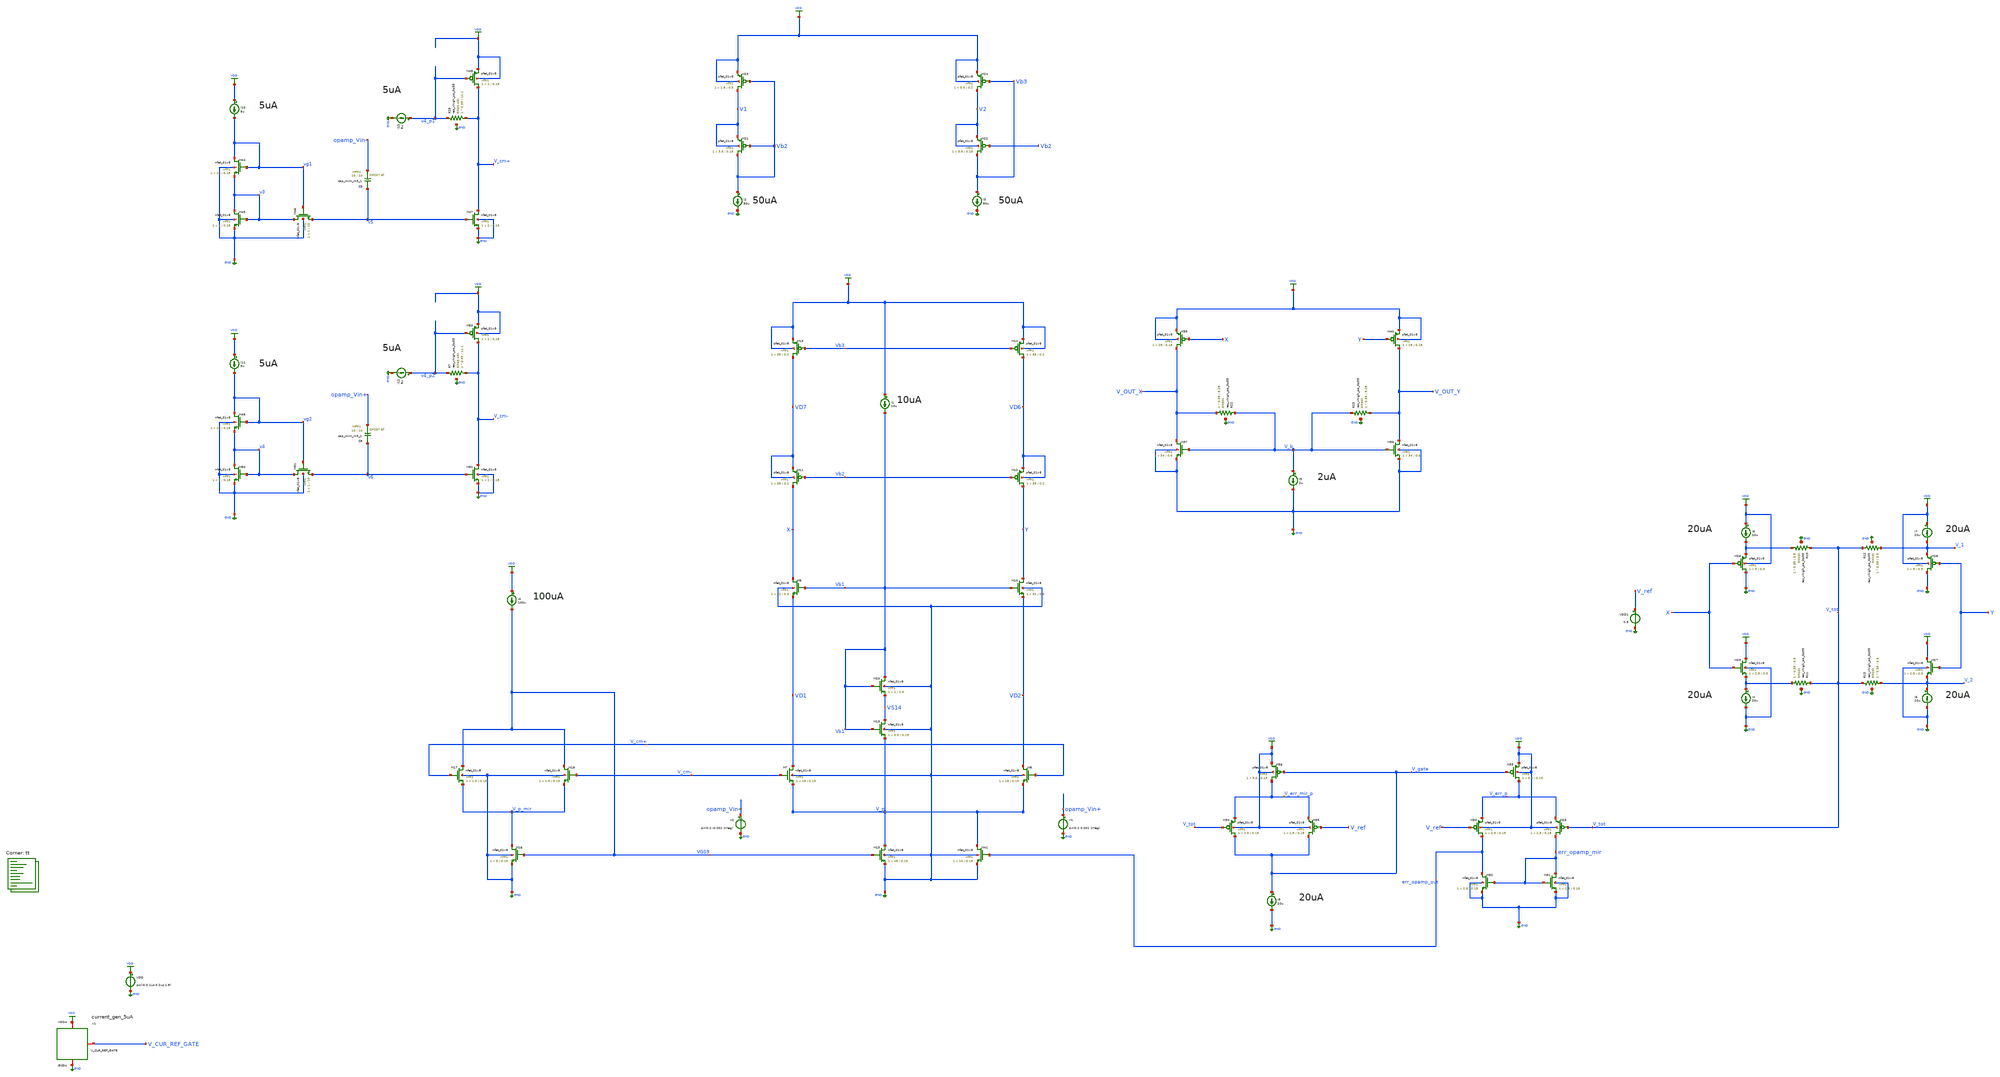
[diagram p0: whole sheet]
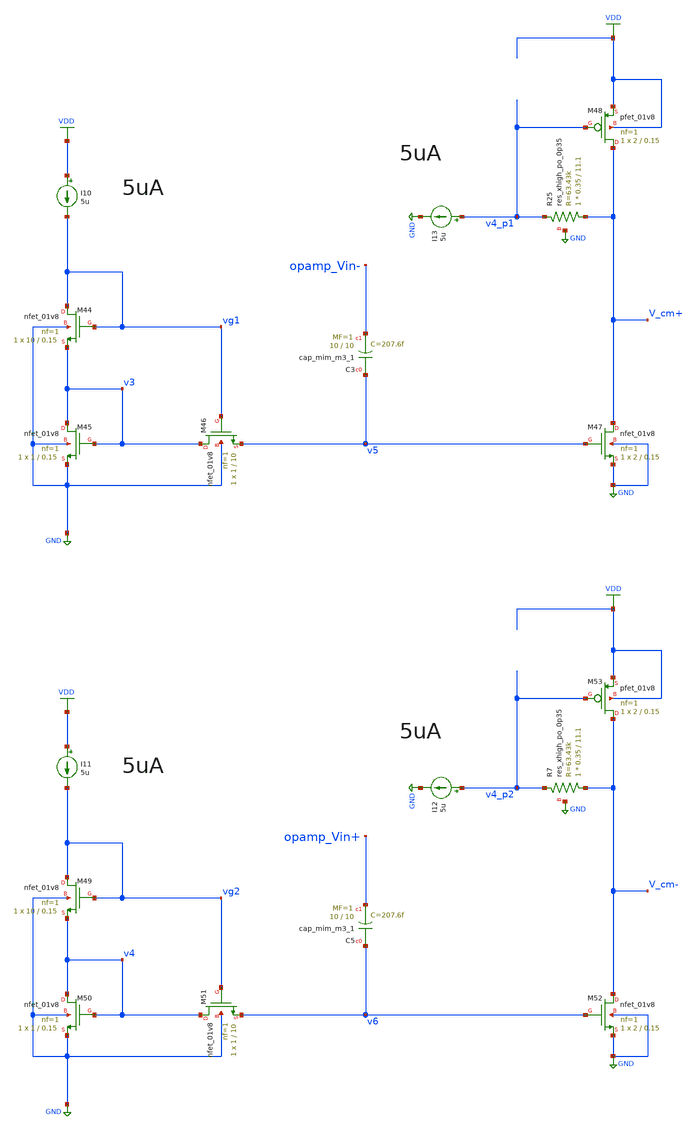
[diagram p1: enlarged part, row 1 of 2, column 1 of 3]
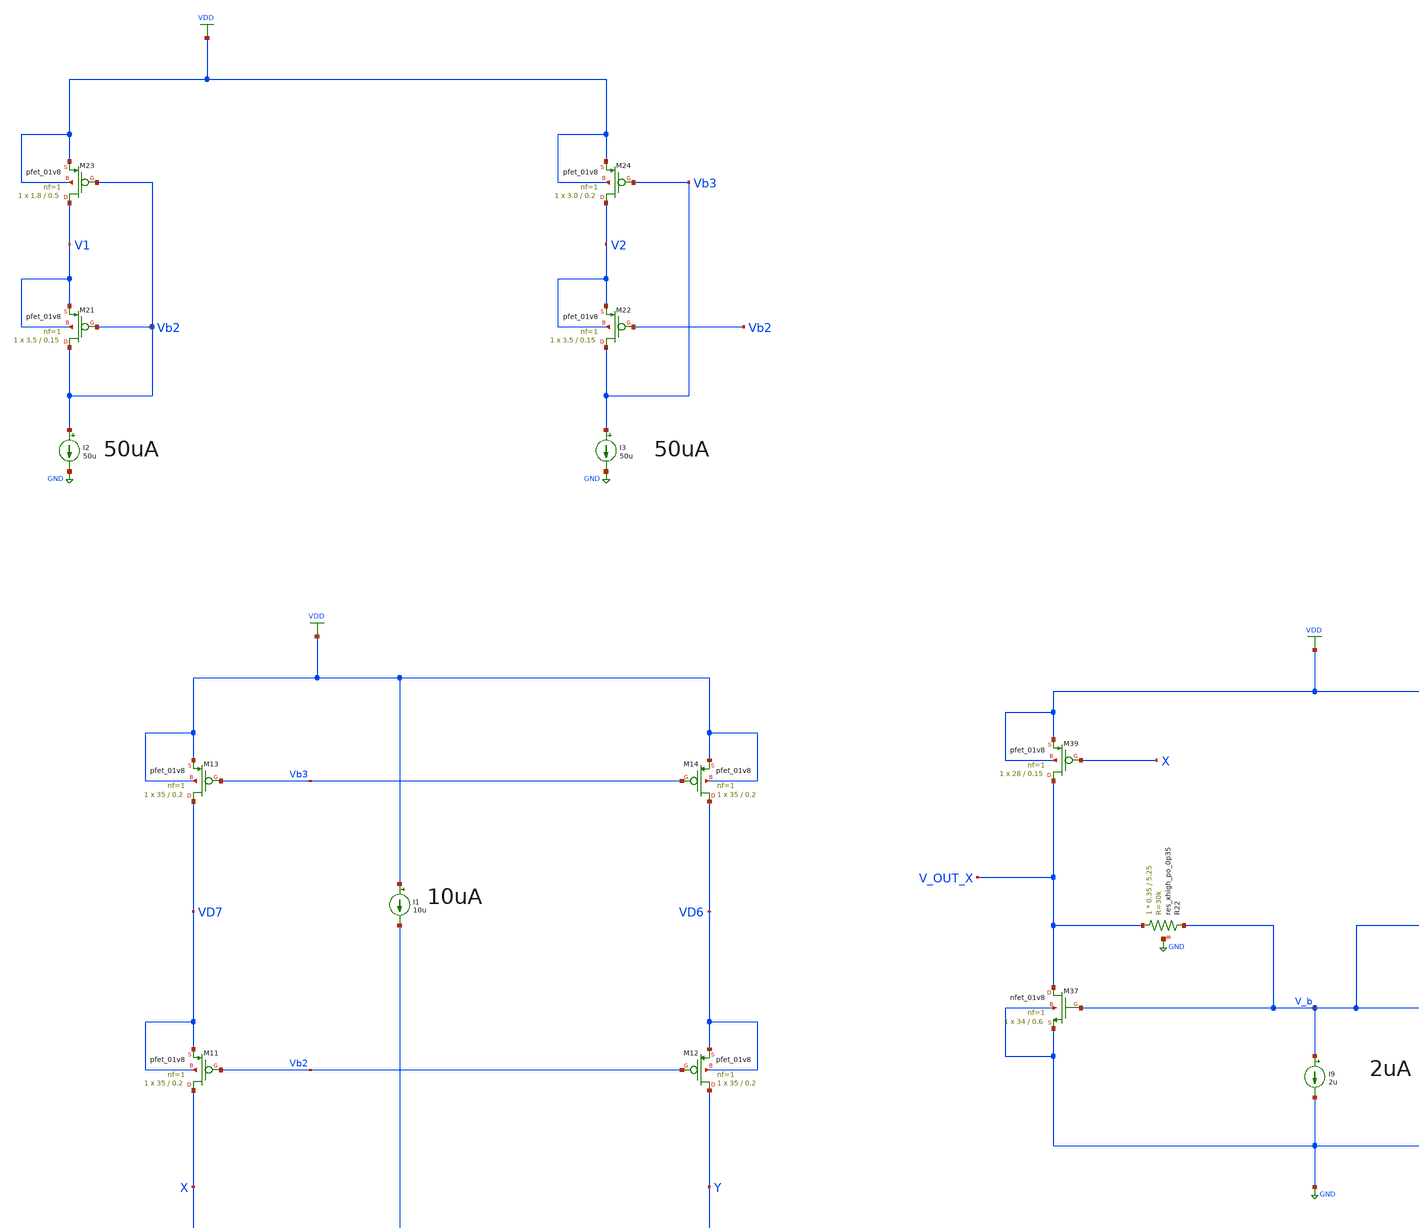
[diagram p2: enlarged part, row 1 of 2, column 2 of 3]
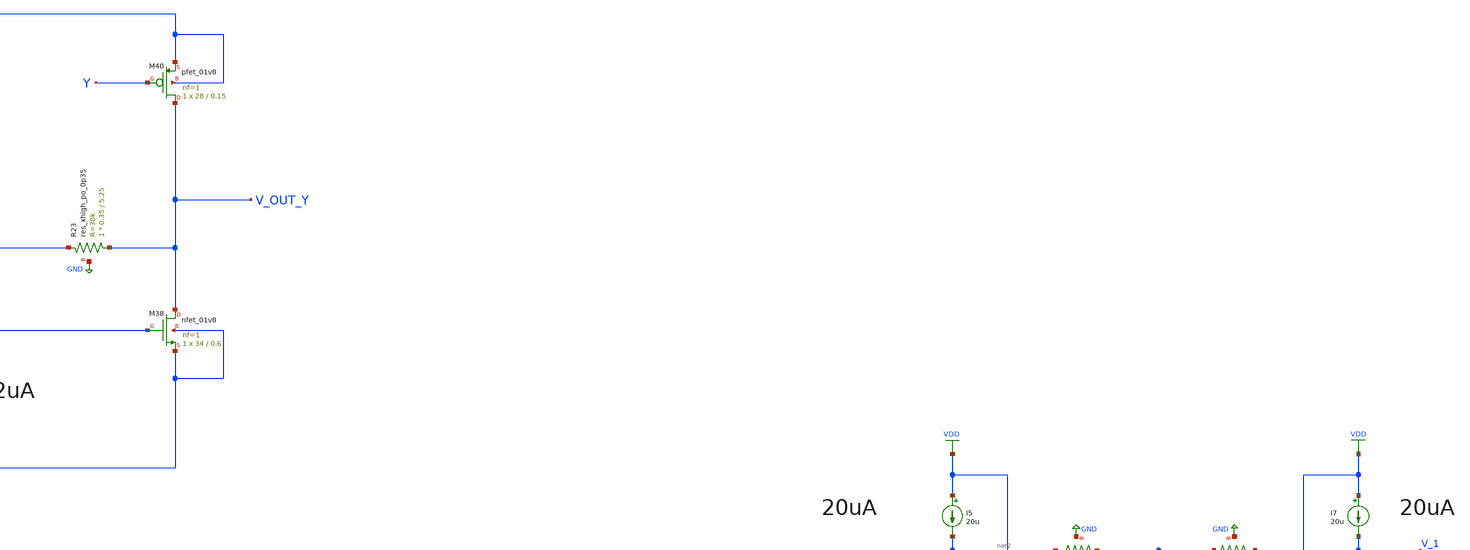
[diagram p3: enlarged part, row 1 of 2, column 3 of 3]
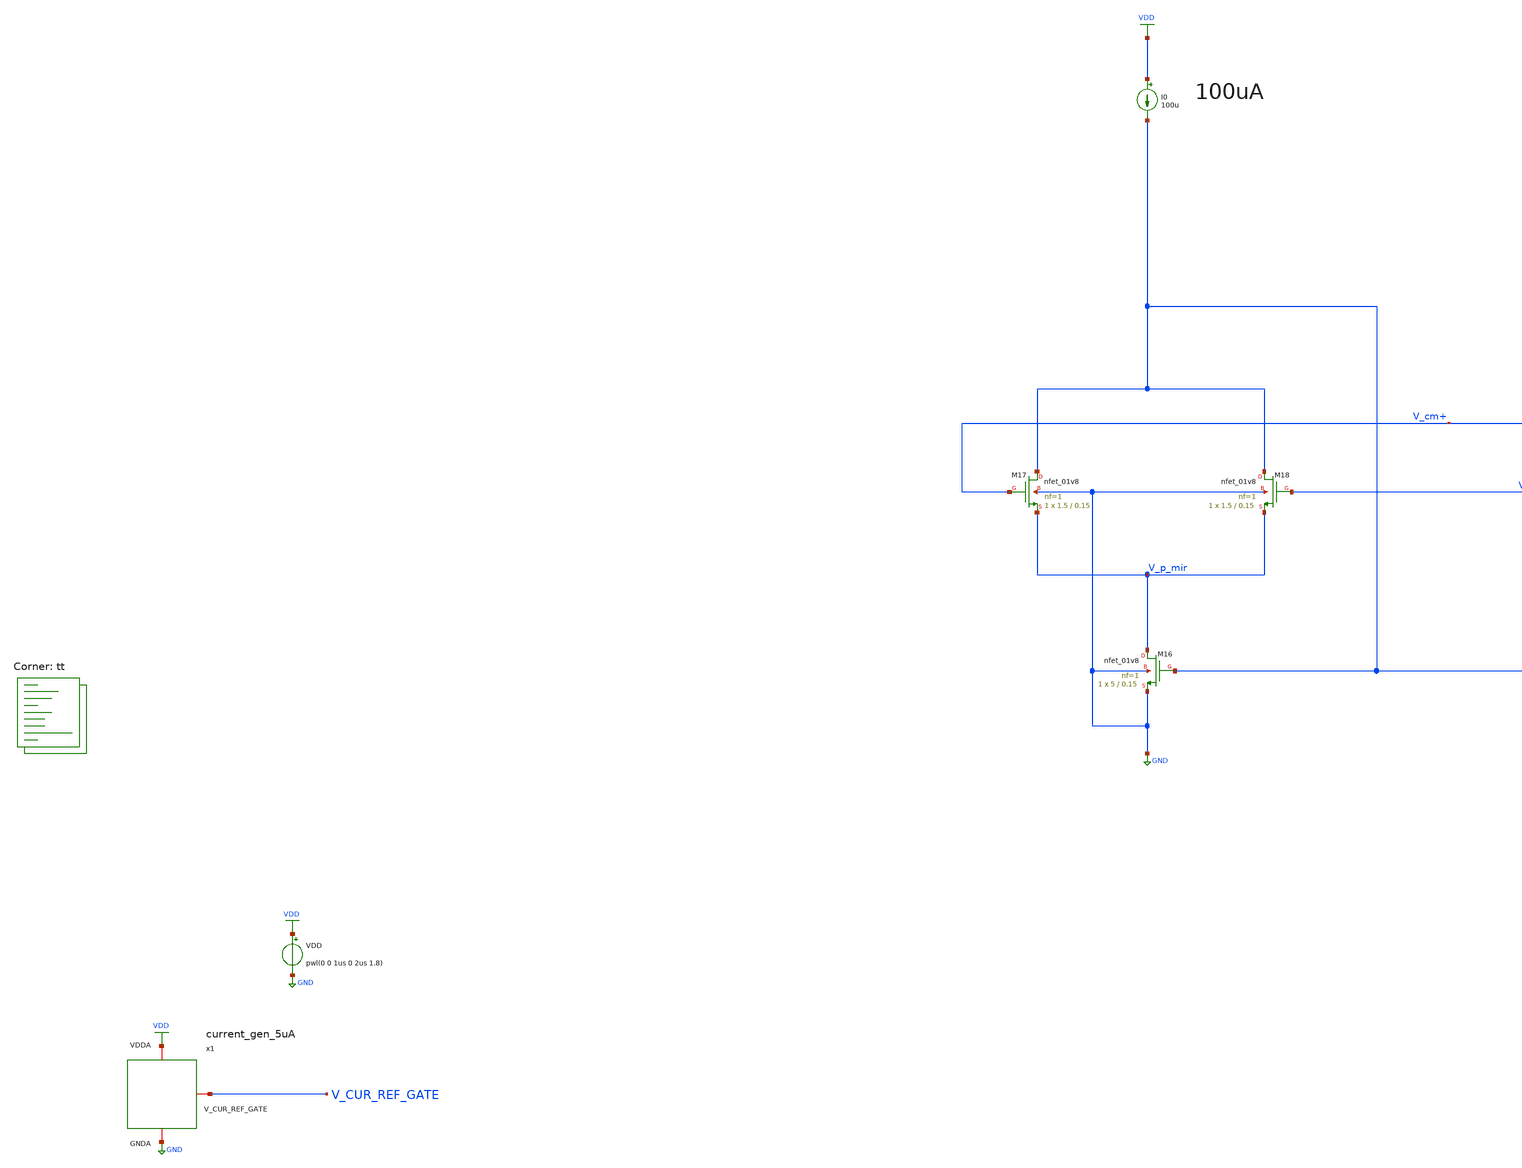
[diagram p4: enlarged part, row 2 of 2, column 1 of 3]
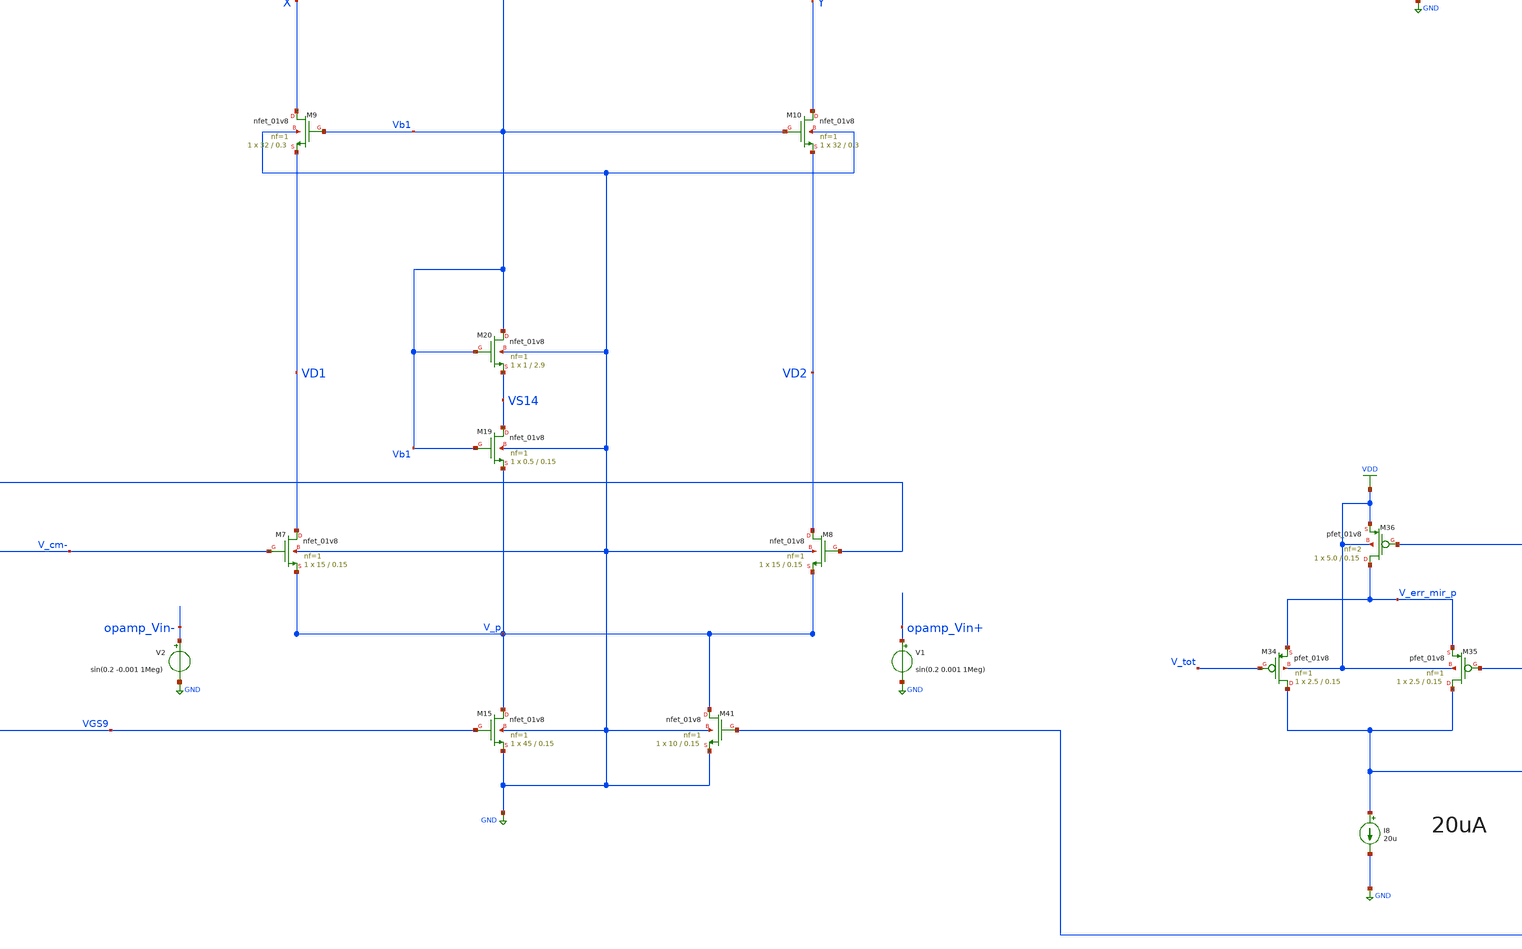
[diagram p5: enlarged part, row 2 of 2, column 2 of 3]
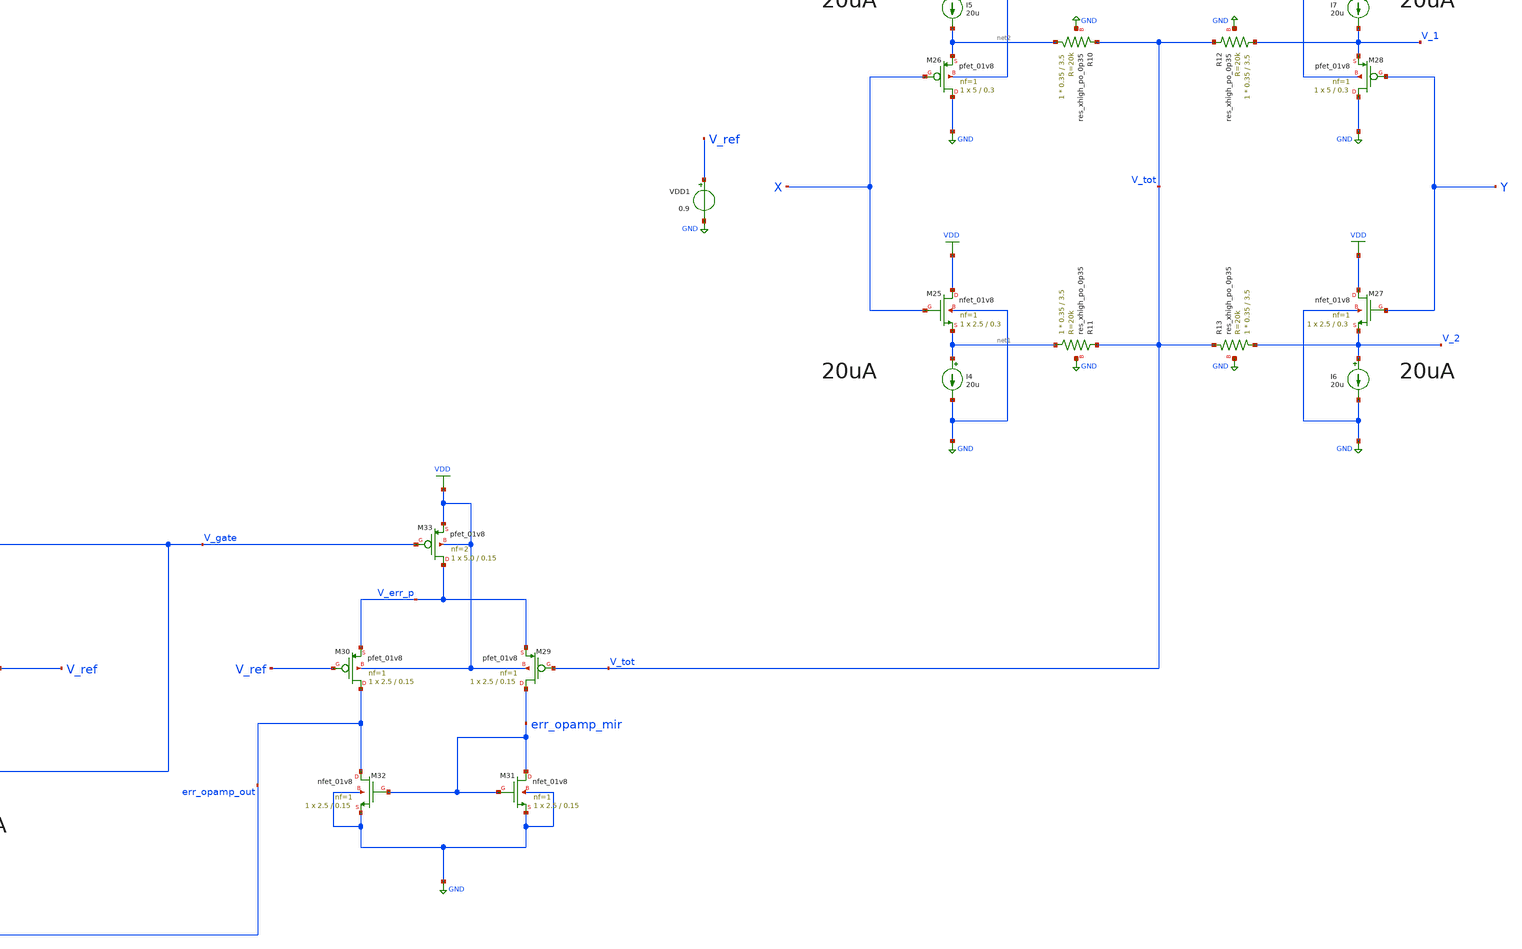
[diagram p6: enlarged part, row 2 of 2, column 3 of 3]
** sch_path: projects/opamp/xschem_ngspice/tb_opamp_ref_cur.sch
**.subckt tb_opamp_ref_cur
VDD VDD GND pwl(0 0 1us 0 2us 1.8)
XM7 VD1 V_cm- V_p GND sky130_fd_pr__nfet_01v8 L=0.15 W=15 nf=1 ad='int((nf+1)/2) * W/nf * 0.29' as='int((nf+2)/2) * W/nf * 0.29'
+ pd='2*int((nf+1)/2) * (W/nf + 0.29)' ps='2*int((nf+2)/2) * (W/nf + 0.29)' nrd='0.29 / W' nrs='0.29 / W'
+ sa=0 sb=0 sd=0 mult=1 m=1
XM8 VD2 V_cm+ V_p GND sky130_fd_pr__nfet_01v8 L=0.15 W=15 nf=1 ad='int((nf+1)/2) * W/nf * 0.29' as='int((nf+2)/2) * W/nf * 0.29'
+ pd='2*int((nf+1)/2) * (W/nf + 0.29)' ps='2*int((nf+2)/2) * (W/nf + 0.29)' nrd='0.29 / W' nrs='0.29 / W'
+ sa=0 sb=0 sd=0 mult=1 m=1
XM9 X Vb1 VD1 GND sky130_fd_pr__nfet_01v8 L=0.3 W=32 nf=1 ad='int((nf+1)/2) * W/nf * 0.29' as='int((nf+2)/2) * W/nf * 0.29'
+ pd='2*int((nf+1)/2) * (W/nf + 0.29)' ps='2*int((nf+2)/2) * (W/nf + 0.29)' nrd='0.29 / W' nrs='0.29 / W'
+ sa=0 sb=0 sd=0 mult=1 m=1
XM10 Y Vb1 VD2 GND sky130_fd_pr__nfet_01v8 L=0.3 W=32 nf=1 ad='int((nf+1)/2) * W/nf * 0.29' as='int((nf+2)/2) * W/nf * 0.29'
+ pd='2*int((nf+1)/2) * (W/nf + 0.29)' ps='2*int((nf+2)/2) * (W/nf + 0.29)' nrd='0.29 / W' nrs='0.29 / W'
+ sa=0 sb=0 sd=0 mult=1 m=1
XM11 X Vb2 VD7 VD7 sky130_fd_pr__pfet_01v8 L=0.2 W=35 nf=1 ad='int((nf+1)/2) * W/nf * 0.29' as='int((nf+2)/2) * W/nf * 0.29'
+ pd='2*int((nf+1)/2) * (W/nf + 0.29)' ps='2*int((nf+2)/2) * (W/nf + 0.29)' nrd='0.29 / W' nrs='0.29 / W'
+ sa=0 sb=0 sd=0 mult=1 m=1
XM12 Y Vb2 VD6 VD6 sky130_fd_pr__pfet_01v8 L=0.2 W=35 nf=1 ad='int((nf+1)/2) * W/nf * 0.29' as='int((nf+2)/2) * W/nf * 0.29'
+ pd='2*int((nf+1)/2) * (W/nf + 0.29)' ps='2*int((nf+2)/2) * (W/nf + 0.29)' nrd='0.29 / W' nrs='0.29 / W'
+ sa=0 sb=0 sd=0 mult=1 m=1
XM13 VD7 Vb3 VDD VDD sky130_fd_pr__pfet_01v8 L=0.2 W=35 nf=1 ad='int((nf+1)/2) * W/nf * 0.29' as='int((nf+2)/2) * W/nf * 0.29'
+ pd='2*int((nf+1)/2) * (W/nf + 0.29)' ps='2*int((nf+2)/2) * (W/nf + 0.29)' nrd='0.29 / W' nrs='0.29 / W'
+ sa=0 sb=0 sd=0 mult=1 m=1
XM14 VD6 Vb3 VDD VDD sky130_fd_pr__pfet_01v8 L=0.2 W=35 nf=1 ad='int((nf+1)/2) * W/nf * 0.29' as='int((nf+2)/2) * W/nf * 0.29'
+ pd='2*int((nf+1)/2) * (W/nf + 0.29)' ps='2*int((nf+2)/2) * (W/nf + 0.29)' nrd='0.29 / W' nrs='0.29 / W'
+ sa=0 sb=0 sd=0 mult=1 m=1
XM15 V_p VGS9 GND GND sky130_fd_pr__nfet_01v8 L=0.15 W=45 nf=1 ad='int((nf+1)/2) * W/nf * 0.29' as='int((nf+2)/2) * W/nf * 0.29'
+ pd='2*int((nf+1)/2) * (W/nf + 0.29)' ps='2*int((nf+2)/2) * (W/nf + 0.29)' nrd='0.29 / W' nrs='0.29 / W'
+ sa=0 sb=0 sd=0 mult=1 m=1
XM16 V_p_mir VGS9 GND GND sky130_fd_pr__nfet_01v8 L=0.15 W=5 nf=1 ad='int((nf+1)/2) * W/nf * 0.29' as='int((nf+2)/2) * W/nf * 0.29'
+ pd='2*int((nf+1)/2) * (W/nf + 0.29)' ps='2*int((nf+2)/2) * (W/nf + 0.29)' nrd='0.29 / W' nrs='0.29 / W'
+ sa=0 sb=0 sd=0 mult=1 m=1
I0 VDD VGS9 100u
XM17 VGS9 V_cm+ V_p_mir GND sky130_fd_pr__nfet_01v8 L=0.15 W=1.5 nf=1 ad='int((nf+1)/2) * W/nf * 0.29'
+ as='int((nf+2)/2) * W/nf * 0.29' pd='2*int((nf+1)/2) * (W/nf + 0.29)' ps='2*int((nf+2)/2) * (W/nf + 0.29)'
+ nrd='0.29 / W' nrs='0.29 / W' sa=0 sb=0 sd=0 mult=1 m=1
XM18 VGS9 V_cm- V_p_mir GND sky130_fd_pr__nfet_01v8 L=0.15 W=1.5 nf=1 ad='int((nf+1)/2) * W/nf * 0.29'
+ as='int((nf+2)/2) * W/nf * 0.29' pd='2*int((nf+1)/2) * (W/nf + 0.29)' ps='2*int((nf+2)/2) * (W/nf + 0.29)'
+ nrd='0.29 / W' nrs='0.29 / W' sa=0 sb=0 sd=0 mult=1 m=1
XM19 VS14 Vb1 V_p GND sky130_fd_pr__nfet_01v8 L=0.15 W=0.5 nf=1 ad='int((nf+1)/2) * W/nf * 0.29' as='int((nf+2)/2) * W/nf * 0.29'
+ pd='2*int((nf+1)/2) * (W/nf + 0.29)' ps='2*int((nf+2)/2) * (W/nf + 0.29)' nrd='0.29 / W' nrs='0.29 / W'
+ sa=0 sb=0 sd=0 mult=1 m=1
XM20 Vb1 Vb1 VS14 GND sky130_fd_pr__nfet_01v8 L=2.9 W=1 nf=1 ad='int((nf+1)/2) * W/nf * 0.29' as='int((nf+2)/2) * W/nf * 0.29'
+ pd='2*int((nf+1)/2) * (W/nf + 0.29)' ps='2*int((nf+2)/2) * (W/nf + 0.29)' nrd='0.29 / W' nrs='0.29 / W'
+ sa=0 sb=0 sd=0 mult=1 m=1
I1 VDD Vb1 10u
XM21 Vb2 Vb2 V1 V1 sky130_fd_pr__pfet_01v8 L=0.15 W=3.5 nf=1 ad='int((nf+1)/2) * W/nf * 0.29' as='int((nf+2)/2) * W/nf * 0.29'
+ pd='2*int((nf+1)/2) * (W/nf + 0.29)' ps='2*int((nf+2)/2) * (W/nf + 0.29)' nrd='0.29 / W' nrs='0.29 / W'
+ sa=0 sb=0 sd=0 mult=1 m=1
XM22 Vb3 Vb2 V2 V2 sky130_fd_pr__pfet_01v8 L=0.15 W=3.5 nf=1 ad='int((nf+1)/2) * W/nf * 0.29' as='int((nf+2)/2) * W/nf * 0.29'
+ pd='2*int((nf+1)/2) * (W/nf + 0.29)' ps='2*int((nf+2)/2) * (W/nf + 0.29)' nrd='0.29 / W' nrs='0.29 / W'
+ sa=0 sb=0 sd=0 mult=1 m=1
XM23 V1 Vb2 VDD VDD sky130_fd_pr__pfet_01v8 L=0.5 W=1.8 nf=1 ad='int((nf+1)/2) * W/nf * 0.29' as='int((nf+2)/2) * W/nf * 0.29'
+ pd='2*int((nf+1)/2) * (W/nf + 0.29)' ps='2*int((nf+2)/2) * (W/nf + 0.29)' nrd='0.29 / W' nrs='0.29 / W'
+ sa=0 sb=0 sd=0 mult=1 m=1
XM24 V2 Vb3 VDD VDD sky130_fd_pr__pfet_01v8 L=0.2 W=3.0 nf=1 ad='int((nf+1)/2) * W/nf * 0.29' as='int((nf+2)/2) * W/nf * 0.29'
+ pd='2*int((nf+1)/2) * (W/nf + 0.29)' ps='2*int((nf+2)/2) * (W/nf + 0.29)' nrd='0.29 / W' nrs='0.29 / W'
+ sa=0 sb=0 sd=0 mult=1 m=1
I2 Vb2 GND 50u
I3 Vb3 GND 50u
XM25 VDD X net1 GND sky130_fd_pr__nfet_01v8 L=0.3 W=2.5 nf=1 ad='int((nf+1)/2) * W/nf * 0.29' as='int((nf+2)/2) * W/nf * 0.29'
+ pd='2*int((nf+1)/2) * (W/nf + 0.29)' ps='2*int((nf+2)/2) * (W/nf + 0.29)' nrd='0.29 / W' nrs='0.29 / W'
+ sa=0 sb=0 sd=0 mult=1 m=1
XM26 GND X net2 VDD sky130_fd_pr__pfet_01v8 L=0.3 W=5 nf=1 ad='int((nf+1)/2) * W/nf * 0.29' as='int((nf+2)/2) * W/nf * 0.29'
+ pd='2*int((nf+1)/2) * (W/nf + 0.29)' ps='2*int((nf+2)/2) * (W/nf + 0.29)' nrd='0.29 / W' nrs='0.29 / W'
+ sa=0 sb=0 sd=0 mult=1 m=1
I4 net1 GND 20u
I5 VDD net2 20u
XR10 net2 V_tot GND sky130_fd_pr__res_xhigh_po_0p35 L=3.5 mult=1 m=1
XR11 net1 V_tot GND sky130_fd_pr__res_xhigh_po_0p35 L=3.5 mult=1 m=1
XR12 V_1 V_tot GND sky130_fd_pr__res_xhigh_po_0p35 L=3.5 mult=1 m=1
XR13 V_2 V_tot GND sky130_fd_pr__res_xhigh_po_0p35 L=3.5 mult=1 m=1
XM27 VDD Y V_2 GND sky130_fd_pr__nfet_01v8 L=0.3 W=2.5 nf=1 ad='int((nf+1)/2) * W/nf * 0.29' as='int((nf+2)/2) * W/nf * 0.29'
+ pd='2*int((nf+1)/2) * (W/nf + 0.29)' ps='2*int((nf+2)/2) * (W/nf + 0.29)' nrd='0.29 / W' nrs='0.29 / W'
+ sa=0 sb=0 sd=0 mult=1 m=1
XM28 GND Y V_1 VDD sky130_fd_pr__pfet_01v8 L=0.3 W=5 nf=1 ad='int((nf+1)/2) * W/nf * 0.29' as='int((nf+2)/2) * W/nf * 0.29'
+ pd='2*int((nf+1)/2) * (W/nf + 0.29)' ps='2*int((nf+2)/2) * (W/nf + 0.29)' nrd='0.29 / W' nrs='0.29 / W'
+ sa=0 sb=0 sd=0 mult=1 m=1
I6 V_2 GND 20u
I7 VDD V_1 20u
XM29 err_opamp_mir V_tot V_err_p VDD sky130_fd_pr__pfet_01v8 L=0.15 W=2.5 nf=1 ad='int((nf+1)/2) * W/nf * 0.29'
+ as='int((nf+2)/2) * W/nf * 0.29' pd='2*int((nf+1)/2) * (W/nf + 0.29)' ps='2*int((nf+2)/2) * (W/nf + 0.29)'
+ nrd='0.29 / W' nrs='0.29 / W' sa=0 sb=0 sd=0 mult=1 m=1
XM30 err_opamp_out V_ref V_err_p VDD sky130_fd_pr__pfet_01v8 L=0.15 W=2.5 nf=1 ad='int((nf+1)/2) * W/nf * 0.29'
+ as='int((nf+2)/2) * W/nf * 0.29' pd='2*int((nf+1)/2) * (W/nf + 0.29)' ps='2*int((nf+2)/2) * (W/nf + 0.29)'
+ nrd='0.29 / W' nrs='0.29 / W' sa=0 sb=0 sd=0 mult=1 m=1
I8 V_gate GND 20u
XM31 err_opamp_mir err_opamp_mir GND GND sky130_fd_pr__nfet_01v8 L=0.15 W=2.5 nf=1 ad='int((nf+1)/2) * W/nf * 0.29'
+ as='int((nf+2)/2) * W/nf * 0.29' pd='2*int((nf+1)/2) * (W/nf + 0.29)' ps='2*int((nf+2)/2) * (W/nf + 0.29)'
+ nrd='0.29 / W' nrs='0.29 / W' sa=0 sb=0 sd=0 mult=1 m=1
XM32 err_opamp_out err_opamp_mir GND GND sky130_fd_pr__nfet_01v8 L=0.15 W=2.5 nf=1 ad='int((nf+1)/2) * W/nf * 0.29'
+ as='int((nf+2)/2) * W/nf * 0.29' pd='2*int((nf+1)/2) * (W/nf + 0.29)' ps='2*int((nf+2)/2) * (W/nf + 0.29)'
+ nrd='0.29 / W' nrs='0.29 / W' sa=0 sb=0 sd=0 mult=1 m=1
VDD1 V_ref GND 0.9
XM33 V_err_p V_gate VDD VDD sky130_fd_pr__pfet_01v8 L=0.15 W=5.0 nf=2 ad='int((nf+1)/2) * W/nf * 0.29'
+ as='int((nf+2)/2) * W/nf * 0.29' pd='2*int((nf+1)/2) * (W/nf + 0.29)' ps='2*int((nf+2)/2) * (W/nf + 0.29)'
+ nrd='0.29 / W' nrs='0.29 / W' sa=0 sb=0 sd=0 mult=1 m=1
XM34 V_gate V_tot V_err_mir_p VDD sky130_fd_pr__pfet_01v8 L=0.15 W=2.5 nf=1 ad='int((nf+1)/2) * W/nf * 0.29'
+ as='int((nf+2)/2) * W/nf * 0.29' pd='2*int((nf+1)/2) * (W/nf + 0.29)' ps='2*int((nf+2)/2) * (W/nf + 0.29)'
+ nrd='0.29 / W' nrs='0.29 / W' sa=0 sb=0 sd=0 mult=1 m=1
XM35 V_gate V_ref V_err_mir_p VDD sky130_fd_pr__pfet_01v8 L=0.15 W=2.5 nf=1 ad='int((nf+1)/2) * W/nf * 0.29'
+ as='int((nf+2)/2) * W/nf * 0.29' pd='2*int((nf+1)/2) * (W/nf + 0.29)' ps='2*int((nf+2)/2) * (W/nf + 0.29)'
+ nrd='0.29 / W' nrs='0.29 / W' sa=0 sb=0 sd=0 mult=1 m=1
XM36 V_err_mir_p V_gate VDD VDD sky130_fd_pr__pfet_01v8 L=0.15 W=5.0 nf=2 ad='int((nf+1)/2) * W/nf * 0.29'
+ as='int((nf+2)/2) * W/nf * 0.29' pd='2*int((nf+1)/2) * (W/nf + 0.29)' ps='2*int((nf+2)/2) * (W/nf + 0.29)'
+ nrd='0.29 / W' nrs='0.29 / W' sa=0 sb=0 sd=0 mult=1 m=1
V2 opamp_Vin- GND sin(0.2 -0.001 1Meg)
V1 opamp_Vin+ GND sin(0.2 0.001 1Meg)
XM37 V_OUT_X V_b GND GND sky130_fd_pr__nfet_01v8 L=0.6 W=34 nf=1 ad='int((nf+1)/2) * W/nf * 0.29' as='int((nf+2)/2) * W/nf * 0.29'
+ pd='2*int((nf+1)/2) * (W/nf + 0.29)' ps='2*int((nf+2)/2) * (W/nf + 0.29)' nrd='0.29 / W' nrs='0.29 / W'
+ sa=0 sb=0 sd=0 mult=1 m=1
XM38 V_OUT_Y V_b GND GND sky130_fd_pr__nfet_01v8 L=0.6 W=34 nf=1 ad='int((nf+1)/2) * W/nf * 0.29' as='int((nf+2)/2) * W/nf * 0.29'
+ pd='2*int((nf+1)/2) * (W/nf + 0.29)' ps='2*int((nf+2)/2) * (W/nf + 0.29)' nrd='0.29 / W' nrs='0.29 / W'
+ sa=0 sb=0 sd=0 mult=1 m=1
XM39 V_OUT_X X VDD VDD sky130_fd_pr__pfet_01v8 L=0.15 W=28 nf=1 ad='int((nf+1)/2) * W/nf * 0.29' as='int((nf+2)/2) * W/nf * 0.29'
+ pd='2*int((nf+1)/2) * (W/nf + 0.29)' ps='2*int((nf+2)/2) * (W/nf + 0.29)' nrd='0.29 / W' nrs='0.29 / W'
+ sa=0 sb=0 sd=0 mult=1 m=1
XM40 V_OUT_Y Y VDD VDD sky130_fd_pr__pfet_01v8 L=0.15 W=28 nf=1 ad='int((nf+1)/2) * W/nf * 0.29' as='int((nf+2)/2) * W/nf * 0.29'
+ pd='2*int((nf+1)/2) * (W/nf + 0.29)' ps='2*int((nf+2)/2) * (W/nf + 0.29)' nrd='0.29 / W' nrs='0.29 / W'
+ sa=0 sb=0 sd=0 mult=1 m=1
XR22 V_OUT_X V_b GND sky130_fd_pr__res_xhigh_po_0p35 L=5.25 mult=1 m=1
XR23 V_OUT_Y V_b GND sky130_fd_pr__res_xhigh_po_0p35 L=5.25 mult=1 m=1
I9 V_b GND 2u
XM41 V_p err_opamp_out GND GND sky130_fd_pr__nfet_01v8 L=0.15 W=10 nf=1 ad='int((nf+1)/2) * W/nf * 0.29'
+ as='int((nf+2)/2) * W/nf * 0.29' pd='2*int((nf+1)/2) * (W/nf + 0.29)' ps='2*int((nf+2)/2) * (W/nf + 0.29)'
+ nrd='0.29 / W' nrs='0.29 / W' sa=0 sb=0 sd=0 mult=1 m=1
I10 VDD vg1 5u
XC3 v5 opamp_Vin- sky130_fd_pr__cap_mim_m3_1 W=10 L=10 MF=1 m=1
XM44 vg1 vg1 v3 GND sky130_fd_pr__nfet_01v8 L=0.15 W=10 nf=1 ad='int((nf+1)/2) * W/nf * 0.29' as='int((nf+2)/2) * W/nf * 0.29'
+ pd='2*int((nf+1)/2) * (W/nf + 0.29)' ps='2*int((nf+2)/2) * (W/nf + 0.29)' nrd='0.29 / W' nrs='0.29 / W'
+ sa=0 sb=0 sd=0 mult=1 m=1
XM45 v3 v3 GND GND sky130_fd_pr__nfet_01v8 L=0.15 W=1 nf=1 ad='int((nf+1)/2) * W/nf * 0.29' as='int((nf+2)/2) * W/nf * 0.29'
+ pd='2*int((nf+1)/2) * (W/nf + 0.29)' ps='2*int((nf+2)/2) * (W/nf + 0.29)' nrd='0.29 / W' nrs='0.29 / W'
+ sa=0 sb=0 sd=0 mult=1 m=1
XM46 v3 vg1 v5 GND sky130_fd_pr__nfet_01v8 L=10 W=1 nf=1 ad='int((nf+1)/2) * W/nf * 0.29' as='int((nf+2)/2) * W/nf * 0.29'
+ pd='2*int((nf+1)/2) * (W/nf + 0.29)' ps='2*int((nf+2)/2) * (W/nf + 0.29)' nrd='0.29 / W' nrs='0.29 / W'
+ sa=0 sb=0 sd=0 mult=1 m=1
XM47 V_cm+ v5 GND GND sky130_fd_pr__nfet_01v8 L=0.15 W=2 nf=1 ad='int((nf+1)/2) * W/nf * 0.29' as='int((nf+2)/2) * W/nf * 0.29'
+ pd='2*int((nf+1)/2) * (W/nf + 0.29)' ps='2*int((nf+2)/2) * (W/nf + 0.29)' nrd='0.29 / W' nrs='0.29 / W'
+ sa=0 sb=0 sd=0 mult=1 m=1
XM48 V_cm+ v4_p1 VDD VDD sky130_fd_pr__pfet_01v8 L=0.15 W=2 nf=1 ad='int((nf+1)/2) * W/nf * 0.29' as='int((nf+2)/2) * W/nf * 0.29'
+ pd='2*int((nf+1)/2) * (W/nf + 0.29)' ps='2*int((nf+2)/2) * (W/nf + 0.29)' nrd='0.29 / W' nrs='0.29 / W'
+ sa=0 sb=0 sd=0 mult=1 m=1
XR25 V_cm+ v4_p1 GND sky130_fd_pr__res_xhigh_po_0p35 L=11.1 mult=1 m=1
I11 VDD vg2 5u
XC5 v6 opamp_Vin+ sky130_fd_pr__cap_mim_m3_1 W=10 L=10 MF=1 m=1
XM49 vg2 vg2 v4 GND sky130_fd_pr__nfet_01v8 L=0.15 W=10 nf=1 ad='int((nf+1)/2) * W/nf * 0.29' as='int((nf+2)/2) * W/nf * 0.29'
+ pd='2*int((nf+1)/2) * (W/nf + 0.29)' ps='2*int((nf+2)/2) * (W/nf + 0.29)' nrd='0.29 / W' nrs='0.29 / W'
+ sa=0 sb=0 sd=0 mult=1 m=1
XM50 v4 v4 GND GND sky130_fd_pr__nfet_01v8 L=0.15 W=1 nf=1 ad='int((nf+1)/2) * W/nf * 0.29' as='int((nf+2)/2) * W/nf * 0.29'
+ pd='2*int((nf+1)/2) * (W/nf + 0.29)' ps='2*int((nf+2)/2) * (W/nf + 0.29)' nrd='0.29 / W' nrs='0.29 / W'
+ sa=0 sb=0 sd=0 mult=1 m=1
XM51 v4 vg2 v6 GND sky130_fd_pr__nfet_01v8 L=10 W=1 nf=1 ad='int((nf+1)/2) * W/nf * 0.29' as='int((nf+2)/2) * W/nf * 0.29'
+ pd='2*int((nf+1)/2) * (W/nf + 0.29)' ps='2*int((nf+2)/2) * (W/nf + 0.29)' nrd='0.29 / W' nrs='0.29 / W'
+ sa=0 sb=0 sd=0 mult=1 m=1
XM52 V_cm- v6 GND GND sky130_fd_pr__nfet_01v8 L=0.15 W=2 nf=1 ad='int((nf+1)/2) * W/nf * 0.29' as='int((nf+2)/2) * W/nf * 0.29'
+ pd='2*int((nf+1)/2) * (W/nf + 0.29)' ps='2*int((nf+2)/2) * (W/nf + 0.29)' nrd='0.29 / W' nrs='0.29 / W'
+ sa=0 sb=0 sd=0 mult=1 m=1
XM53 V_cm- v4_p2 VDD VDD sky130_fd_pr__pfet_01v8 L=0.15 W=2 nf=1 ad='int((nf+1)/2) * W/nf * 0.29' as='int((nf+2)/2) * W/nf * 0.29'
+ pd='2*int((nf+1)/2) * (W/nf + 0.29)' ps='2*int((nf+2)/2) * (W/nf + 0.29)' nrd='0.29 / W' nrs='0.29 / W'
+ sa=0 sb=0 sd=0 mult=1 m=1
XR7 V_cm- v4_p2 GND sky130_fd_pr__res_xhigh_po_0p35 L=11.1 mult=1 m=1
I12 v4_p2 GND 5u
I13 v4_p1 GND 5u
x1 VDD V_CUR_REF_GATE GND current_gen_5uA
**** begin user architecture code
.lib $::SKYWATER_MODELS/sky130.lib.spice tt



.option method=gear
.option wnflag=1
.option savecurrents

.save @m.xm7.msky130_fd_pr__nfet_01v8[gm] @m.xm7.msky130_fd_pr__nfet_01v8[vth] @m.xm8.msky130_fd_pr__nfet_01v8[gm] @m.xm8.msky130_fd_pr__nfet_01v8[vth] @m.xm8.msky130_fd_pr__nfet_01v8[gm] @m.xm8.msky130_fd_pr__nfet_01v8[vth] @m.xm9.msky130_fd_pr__nfet_01v8[gm] @m.xm9.msky130_fd_pr__nfet_01v8[vth] @m.xm10.msky130_fd_pr__pfet_01v8[gm] @m.xm10.msky130_fd_pr__pfet_01v8[vth] @m.xm11.msky130_fd_pr__pfet_01v8[gm] @m.xm11.msky130_fd_pr__pfet_01v8[vth] @m.xm12.msky130_fd_pr__pfet_01v8[gm] @m.xm12.msky130_fd_pr__pfet_01v8[vth] @m.xm13.msky130_fd_pr__pfet_01v8[gm] @m.xm13.msky130_fd_pr__pfet_01v8[vth] @m.xm14.msky130_fd_pr__nfet_01v8[gm] @m.xm14.msky130_fd_pr__nfet_01v8[vth] @m.xm15.msky130_fd_pr__nfet_01v8[gm] @m.xm15.msky130_fd_pr__nfet_01v8[vth] @m.xm16.msky130_fd_pr__nfet_01v8[gm] @m.xm16.msky130_fd_pr__nfet_01v8[vth] @m.xm17.msky130_fd_pr__nfet_01v8[gm] @m.xm17.msky130_fd_pr__nfet_01v8[vth] @m.xm18.msky130_fd_pr__nfet_01v8[gm] @m.xm18.msky130_fd_pr__nfet_01v8[vth] @m.xm19.msky130_fd_pr__nfet_01v8[gm] @m.xm19.msky130_fd_pr__nfet_01v8[vth] @m.xm20.msky130_fd_pr__nfet_01v8[gm] @m.xm20.msky130_fd_pr__nfet_01v8[vth] @m.xm21.msky130_fd_pr__pfet_01v8[gm] @m.xm21.msky130_fd_pr__pfet_01v8[vth] @m.xm22.msky130_fd_pr__pfet_01v8[gm] @m.xm22.msky130_fd_pr__pfet_01v8[vth] @m.xm23.msky130_fd_pr__pfet_01v8[gm] @m.xm23.msky130_fd_pr__pfet_01v8[vth] @m.xm24.msky130_fd_pr__pfet_01v8[gm] @m.xm24.msky130_fd_pr__pfet_01v8[vth] @m.xm25.msky130_fd_pr__nfet_01v8[gm] @m.xm25.msky130_fd_pr__nfet_01v8[vth] @m.xm26.msky130_fd_pr__pfet_01v8[gm] @m.xm26.msky130_fd_pr__pfet_01v8[vth] @m.xm27.msky130_fd_pr__nfet_01v8[gm] @m.xm27.msky130_fd_pr__nfet_01v8[vth] @m.xm28.msky130_fd_pr__pfet_01v8[gm] @m.xm28.msky130_fd_pr__pfet_01v8[vth] @m.xm29.msky130_fd_pr__pfet_01v8[gm] @m.xm29.msky130_fd_pr__pfet_01v8[vth] @m.xm30.msky130_fd_pr__pfet_01v8[gm] @m.xm30.msky130_fd_pr__pfet_01v8[vth] @m.xm31.msky130_fd_pr__nfet_01v8[gm] @m.xm31.msky130_fd_pr__nfet_01v8[vth] @m.xm32.msky130_fd_pr__nfet_01v8[gm] @m.xm32.msky130_fd_pr__nfet_01v8[vth] @m.xm33.msky130_fd_pr__pfet_01v8[gm] @m.xm33.msky130_fd_pr__pfet_01v8[vth] @m.xm34.msky130_fd_pr__pfet_01v8[gm] @m.xm34.msky130_fd_pr__pfet_01v8[vth] @m.xm35.msky130_fd_pr__pfet_01v8[gm] @m.xm35.msky130_fd_pr__pfet_01v8[vth] @m.xm36.msky130_fd_pr__pfet_01v8[gm] @m.xm36.msky130_fd_pr__pfet_01v8[vth] @m.xm37.msky130_fd_pr__nfet_01v8[gm] @m.xm37.msky130_fd_pr__nfet_01v8[vth] @m.xm38.msky130_fd_pr__nfet_01v8[gm] @m.xm38.msky130_fd_pr__nfet_01v8[vth] @m.xm39.msky130_fd_pr__pfet_01v8[gm] @m.xm39.msky130_fd_pr__pfet_01v8[vth] @m.xm40.msky130_fd_pr__pfet_01v8[gm] @m.xm40.msky130_fd_pr__pfet_01v8[vth] @m.xm41.msky130_fd_pr__nfet_01v8[gm] @m.xm41.msky130_fd_pr__nfet_01v8[vth] @m.xm42.msky130_fd_pr__nfet_01v8[gm] @m.xm42.msky130_fd_pr__nfet_01v8[vth] @m.xm43.msky130_fd_pr__nfet_01v8[gm] @m.xm43.msky130_fd_pr__nfet_01v8[vth] @m.x1.xm1.msky130_fd_pr__pfet_01v8[gm] @m.x1.xm1.msky130_fd_pr__pfet_01v8[vth] @m.x1.xm2.msky130_fd_pr__pfet_01v8[gm] @m.x1.xm2.msky130_fd_pr__pfet_01v8[vth] @m.x1.xm3.msky130_fd_pr__pfet_01v8[gm] @m.x1.xm3.msky130_fd_pr__pfet_01v8[vth] @m.x1.xm4.msky130_fd_pr__pfet_01v8[gm] @m.x1.xm4.msky130_fd_pr__pfet_01v8[vth] @m.x1.xm5.msky130_fd_pr__nfet_01v8[gm] @m.x1.xm5.msky130_fd_pr__nfet_01v8[vth] @m.x1.xm6.msky130_fd_pr__pfet_01v8[gm] @m.x1.xm6.msky130_fd_pr__pfet_01v8[vth] @m.x1.xm7.msky130_fd_pr__nfet_01v8[gm] @m.x1.xm7.msky130_fd_pr__nfet_01v8[vth] @m.x1.xm8.msky130_fd_pr__pfet_01v8[gm] @m.x1.xm8.msky130_fd_pr__pfet_01v8[vth] @m.x1.x1.xm1.msky130_fd_pr__nfet_01v8[gm] @m.x1.x1.xm2.msky130_fd_pr__nfet_01v8[gm] @m.x1.x1.xm3.msky130_fd_pr__nfet_01v8[gm] @m.x1.x1.xm4.msky130_fd_pr__nfet_01v8[gm] @m.x1.x1.xm5.msky130_fd_pr__pfet_01v8[gm] @m.x1.x1.xm6.msky130_fd_pr__nfet_01v8[gm] @m.x1.x1.xm7.msky130_fd_pr__pfet_01v8[gm] @m.x1.x2.xm1.msky130_fd_pr__nfet_01v8[gm] @m.x1.x2.xm2.msky130_fd_pr__nfet_01v8[gm] @m.x1.x2.xm3.msky130_fd_pr__nfet_01v8[gm] @m.x1.x2.xm4.msky130_fd_pr__nfet_01v8[gm] @m.x1.x2.xm5.msky130_fd_pr__pfet_01v8[gm] @m.x1.x2.xm6.msky130_fd_pr__nfet_01v8[gm] @m.x1.x2.xm7.msky130_fd_pr__pfet_01v8[gm]

* .ic v(v_top) = 1.8

.control

  save all
  * dc V1 1.238 1.242 0.0001
  * dc VDD 0 1.8 0.9
  * dc temp -40 120 10 VDD 0 4.0 0.2
  * dc VDD 0 2.0 0.02 temp -40 120 40
  * dc VDD 0 2.0 0.01
  * tran 0.4n 3u
  tran 1ns 10us
  * ac dec 20 1 1T
  remzerovec
  write tb_opamp_ref_cur.raw
  set appendwrite
  let first_out = x - y
  let second_out = v_out_x - v_out_y

.endc





**** end user architecture code
**.ends

* expanding   symbol:  current_gen_5uA.sym # of pins=3
** sym_path: projects/bandgapref/xschem_ngspice/new_files/current_gen_5uA.sym
** sch_path: projects/bandgapref/xschem_ngspice/new_files/current_gen_5uA.sch
.subckt current_gen_5uA VDDA V_CUR_REF_GATE GNDA
*.iopin VDDA
*.iopin GNDA
*.opin V_CUR_REF_GATE
XQ1 GNDA GNDA Vin- sky130_fd_pr__pnp_05v5_W3p40L3p40 m=1
XQ2 GNDA GNDA Vbe2 sky130_fd_pr__pnp_05v5_W3p40L3p40 m=8
XM1 Vin- V_TOP VDDA VDDA sky130_fd_pr__pfet_01v8 L=0.3 W=10 nf=1 ad='int((nf+1)/2) * W/nf * 0.29' as='int((nf+2)/2) * W/nf * 0.29'
+ pd='2*int((nf+1)/2) * (W/nf + 0.29)' ps='2*int((nf+2)/2) * (W/nf + 0.29)' nrd='0.29 / W' nrs='0.29 / W'
+ sa=0 sb=0 sd=0 mult=1 m=1
XM2 Vin+ V_TOP VDDA VDDA sky130_fd_pr__pfet_01v8 L=0.3 W=10 nf=1 ad='int((nf+1)/2) * W/nf * 0.29' as='int((nf+2)/2) * W/nf * 0.29'
+ pd='2*int((nf+1)/2) * (W/nf + 0.29)' ps='2*int((nf+2)/2) * (W/nf + 0.29)' nrd='0.29 / W' nrs='0.29 / W'
+ sa=0 sb=0 sd=0 mult=1 m=1
XM3 V_REF V_TOP VDDA VDDA sky130_fd_pr__pfet_01v8 L=0.3 W=10 nf=1 ad='int((nf+1)/2) * W/nf * 0.29' as='int((nf+2)/2) * W/nf * 0.29'
+ pd='2*int((nf+1)/2) * (W/nf + 0.29)' ps='2*int((nf+2)/2) * (W/nf + 0.29)' nrd='0.29 / W' nrs='0.29 / W'
+ sa=0 sb=0 sd=0 mult=1 m=1
XR1 Vbe2 Vin+ GNDA sky130_fd_pr__res_xhigh_po_0p35 L=3.87 mult=1 m=1
XR2 GNDA Vin+ GNDA sky130_fd_pr__res_xhigh_po_0p35 L=32 mult=1 m=1
XR3 GNDA Vin- GNDA sky130_fd_pr__res_xhigh_po_0p35 L=32 mult=1 m=1
XR4 GNDA V_REF GNDA sky130_fd_pr__res_xhigh_po_0p35 L=32 mult=1 m=1
XM5 start_up start_up start_up_nfet1 start_up_nfet1 sky130_fd_pr__nfet_01v8 L=10 W=1 nf=1 ad='int((nf+1)/2) * W/nf * 0.29'
+ as='int((nf+2)/2) * W/nf * 0.29' pd='2*int((nf+1)/2) * (W/nf + 0.29)' ps='2*int((nf+2)/2) * (W/nf + 0.29)'
+ nrd='0.29 / W' nrs='0.29 / W' sa=0 sb=0 sd=0 mult=1 m=1
XM6 start_up V_TOP VDDA VDDA sky130_fd_pr__pfet_01v8 L=0.3 W=10 nf=1 ad='int((nf+1)/2) * W/nf * 0.29'
+ as='int((nf+2)/2) * W/nf * 0.29' pd='2*int((nf+1)/2) * (W/nf + 0.29)' ps='2*int((nf+2)/2) * (W/nf + 0.29)'
+ nrd='0.29 / W' nrs='0.29 / W' sa=0 sb=0 sd=0 mult=1 m=1
XM4 Vin- start_up V_TOP VDDA sky130_fd_pr__pfet_01v8 L=0.15 W=2 nf=1 ad='int((nf+1)/2) * W/nf * 0.29'
+ as='int((nf+2)/2) * W/nf * 0.29' pd='2*int((nf+1)/2) * (W/nf + 0.29)' ps='2*int((nf+2)/2) * (W/nf + 0.29)'
+ nrd='0.29 / W' nrs='0.29 / W' sa=0 sb=0 sd=0 mult=1 m=1
x1 VDDA V_TOP Vin- Vin+ GNDA opamp_bandgap_2
XM7 start_up_nfet1 start_up_nfet1 GNDA GNDA sky130_fd_pr__nfet_01v8 L=10 W=1 nf=1 ad='int((nf+1)/2) * W/nf * 0.29'
+ as='int((nf+2)/2) * W/nf * 0.29' pd='2*int((nf+1)/2) * (W/nf + 0.29)' ps='2*int((nf+2)/2) * (W/nf + 0.29)'
+ nrd='0.29 / W' nrs='0.29 / W' sa=0 sb=0 sd=0 mult=1 m=1
x2 VDD V_CUR_REF_GATE V_REF V_CUR_REF_REG GND opamp_bandgap_2
XR6 GNDA V_CUR_REF_REG GND sky130_fd_pr__res_xhigh_po_0p35 L=32 mult=1 m=1
XM8 V_CUR_REF_REG V_CUR_REF_GATE VDDA VDDA sky130_fd_pr__pfet_01v8 L=0.3 W=10 nf=1 ad='int((nf+1)/2) * W/nf * 0.29'
+ as='int((nf+2)/2) * W/nf * 0.29' pd='2*int((nf+1)/2) * (W/nf + 0.29)' ps='2*int((nf+2)/2) * (W/nf + 0.29)'
+ nrd='0.29 / W' nrs='0.29 / W' sa=0 sb=0 sd=0 mult=1 m=1
.ends


* expanding   symbol:  opamp_bandgap_2.sym # of pins=5
** sym_path: projects/bandgapref/xschem_ngspice/new_files/opamp_bandgap_2.sym
** sch_path: projects/bandgapref/xschem_ngspice/new_files/opamp_bandgap_2.sch
.subckt opamp_bandgap_2 VDDA Vout Vin- Vin+ GNDA
*.ipin Vin+
*.opin Vout
*.ipin Vin-
*.ipin GNDA
*.ipin VDDA
XM1 V_p VDDA GNDA GNDA sky130_fd_pr__nfet_01v8 L=10 W=5 nf=1 ad='int((nf+1)/2) * W/nf * 0.29' as='int((nf+2)/2) * W/nf * 0.29'
+ pd='2*int((nf+1)/2) * (W/nf + 0.29)' ps='2*int((nf+2)/2) * (W/nf + 0.29)' nrd='0.29 / W' nrs='0.29 / W'
+ sa=0 sb=0 sd=0 mult=1 m=1
XM2 V_mirror Vin- V_p GNDA sky130_fd_pr__nfet_01v8 L=0.2 W=5 nf=1 ad='int((nf+1)/2) * W/nf * 0.29' as='int((nf+2)/2) * W/nf * 0.29'
+ pd='2*int((nf+1)/2) * (W/nf + 0.29)' ps='2*int((nf+2)/2) * (W/nf + 0.29)' nrd='0.29 / W' nrs='0.29 / W'
+ sa=0 sb=0 sd=0 mult=1 m=1
XM3 1st_Vout Vin+ V_p GNDA sky130_fd_pr__nfet_01v8 L=0.2 W=5 nf=1 ad='int((nf+1)/2) * W/nf * 0.29' as='int((nf+2)/2) * W/nf * 0.29'
+ pd='2*int((nf+1)/2) * (W/nf + 0.29)' ps='2*int((nf+2)/2) * (W/nf + 0.29)' nrd='0.29 / W' nrs='0.29 / W'
+ sa=0 sb=0 sd=0 mult=1 m=1
XM5 V_mirror V_mirror VDDA VDDA sky130_fd_pr__pfet_01v8 L=0.2 W=10 nf=2 ad='int((nf+1)/2) * W/nf * 0.29'
+ as='int((nf+2)/2) * W/nf * 0.29' pd='2*int((nf+1)/2) * (W/nf + 0.29)' ps='2*int((nf+2)/2) * (W/nf + 0.29)'
+ nrd='0.29 / W' nrs='0.29 / W' sa=0 sb=0 sd=0 mult=1 m=1
XM6 1st_Vout V_mirror VDDA VDDA sky130_fd_pr__pfet_01v8 L=0.2 W=10 nf=2 ad='int((nf+1)/2) * W/nf * 0.29'
+ as='int((nf+2)/2) * W/nf * 0.29' pd='2*int((nf+1)/2) * (W/nf + 0.29)' ps='2*int((nf+2)/2) * (W/nf + 0.29)'
+ nrd='0.29 / W' nrs='0.29 / W' sa=0 sb=0 sd=0 mult=1 m=1
XM4 Vout VDDA GNDA GNDA sky130_fd_pr__nfet_01v8 L=10 W=5 nf=1 ad='int((nf+1)/2) * W/nf * 0.29' as='int((nf+2)/2) * W/nf * 0.29'
+ pd='2*int((nf+1)/2) * (W/nf + 0.29)' ps='2*int((nf+2)/2) * (W/nf + 0.29)' nrd='0.29 / W' nrs='0.29 / W'
+ sa=0 sb=0 sd=0 mult=1 m=1
XM7 Vout 1st_Vout VDDA VDDA sky130_fd_pr__pfet_01v8 L=0.2 W=10 nf=2 ad='int((nf+1)/2) * W/nf * 0.29'
+ as='int((nf+2)/2) * W/nf * 0.29' pd='2*int((nf+1)/2) * (W/nf + 0.29)' ps='2*int((nf+2)/2) * (W/nf + 0.29)'
+ nrd='0.29 / W' nrs='0.29 / W' sa=0 sb=0 sd=0 mult=1 m=1
.ends

.GLOBAL GND
.GLOBAL VDD
.end
